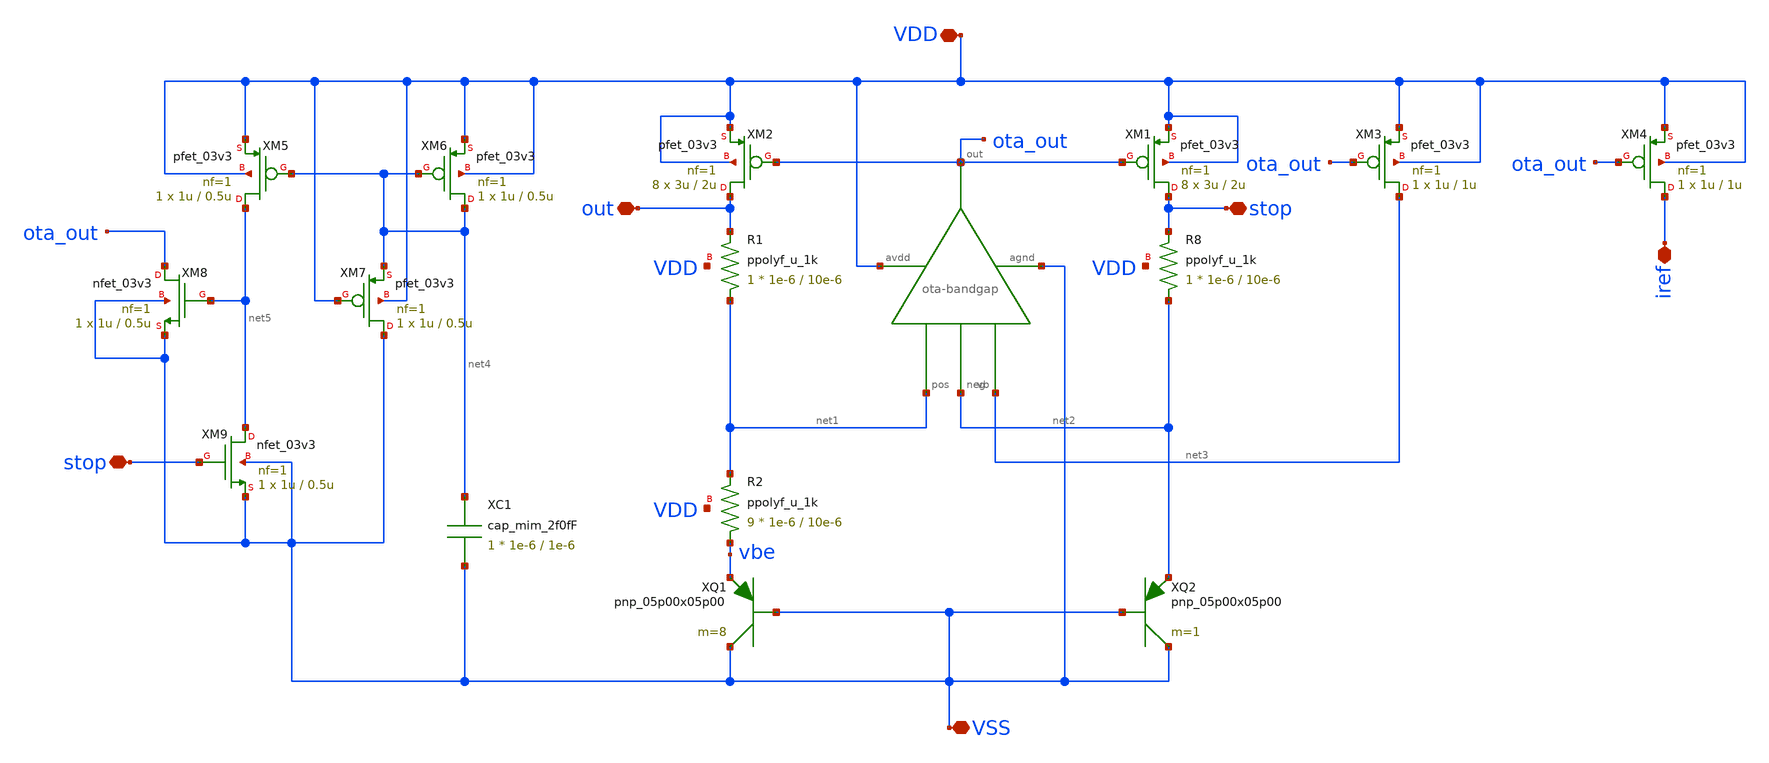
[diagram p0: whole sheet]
** sch_path: LDO/xschem/bandgap/symbol/bandgap.sch

.include $env(PDK_ROOT)/$env(PDK)/libs.tech/ngspice/design.ngspice
.lib $env(PDK_ROOT)/$env(PDK)/libs.tech/ngspice/sm141064.ngspice typical
.lib $env(PDK_ROOT)/$env(PDK)/libs.tech/ngspice/sm141064.ngspice mimcap_statistical
.lib $env(PDK_ROOT)/$env(PDK)/libs.tech/ngspice/sm141064.ngspice cap_mim
.lib $env(PDK_ROOT)/$env(PDK)/libs.tech/ngspice/sm141064.ngspice res_typical
.lib $env(PDK_ROOT)/$env(PDK)/libs.tech/ngspice/sm141064.ngspice bjt_typical
.lib $env(PDK_ROOT)/$env(PDK)/libs.tech/ngspice/sm141064.ngspice moscap_typical

**.subckt bandgap VDD VSS out iref stop stop
*.iopin VDD
*.iopin VSS
*.iopin out
*.iopin iref
*.iopin stop
*.iopin stop
XM1 stop ota_out VDD VDD pfet_03v3 L=2u W=3u nf=1 ad='int((nf+1)/2) * W/nf * 0.18u' as='int((nf+2)/2) * W/nf * 0.18u'
+ pd='2*int((nf+1)/2) * (W/nf + 0.18u)' ps='2*int((nf+2)/2) * (W/nf + 0.18u)' nrd='0.18u / W' nrs='0.18u / W'
+ sa=0 sb=0 sd=0 m=8
XM2 out ota_out VDD VDD pfet_03v3 L=2u W=3u nf=1 ad='int((nf+1)/2) * W/nf * 0.18u' as='int((nf+2)/2) * W/nf * 0.18u'
+ pd='2*int((nf+1)/2) * (W/nf + 0.18u)' ps='2*int((nf+2)/2) * (W/nf + 0.18u)' nrd='0.18u / W' nrs='0.18u / W'
+ sa=0 sb=0 sd=0 m=8
X1 ota_out VSS VDD net1 net2 net3 ota-bandgap
XQ1 VSS VSS vbe pnp_05p00x05p00 m=8
XQ2 VSS VSS net2 pnp_05p00x05p00 m=1
XR8 net2 stop VDD ppolyf_u_1k r_width=1e-6 r_length=10e-6 m=1
XR1 net1 out VDD ppolyf_u_1k r_width=1e-6 r_length=10e-6 m=1
XR2 vbe net1 VDD ppolyf_u_1k r_width=1e-6 r_length=10e-6 m=9
XM3 net3 ota_out VDD VDD pfet_03v3 L=1u W=1u nf=1 ad='int((nf+1)/2) * W/nf * 0.18u' as='int((nf+2)/2) * W/nf * 0.18u'
+ pd='2*int((nf+1)/2) * (W/nf + 0.18u)' ps='2*int((nf+2)/2) * (W/nf + 0.18u)' nrd='0.18u / W' nrs='0.18u / W'
+ sa=0 sb=0 sd=0 m=1
XM4 iref ota_out VDD VDD pfet_03v3 L=1u W=1u nf=1 ad='int((nf+1)/2) * W/nf * 0.18u' as='int((nf+2)/2) * W/nf * 0.18u'
+ pd='2*int((nf+1)/2) * (W/nf + 0.18u)' ps='2*int((nf+2)/2) * (W/nf + 0.18u)' nrd='0.18u / W' nrs='0.18u / W'
+ sa=0 sb=0 sd=0 m=1
XM6 net4 net4 VDD VDD pfet_03v3 L=0.5u W=1u nf=1 ad='int((nf+1)/2) * W/nf * 0.18u' as='int((nf+2)/2) * W/nf * 0.18u'
+ pd='2*int((nf+1)/2) * (W/nf + 0.18u)' ps='2*int((nf+2)/2) * (W/nf + 0.18u)' nrd='0.18u / W' nrs='0.18u / W'
+ sa=0 sb=0 sd=0 m=1
XM5 net5 net4 VDD VDD pfet_03v3 L=0.5u W=1u nf=1 ad='int((nf+1)/2) * W/nf * 0.18u' as='int((nf+2)/2) * W/nf * 0.18u'
+ pd='2*int((nf+1)/2) * (W/nf + 0.18u)' ps='2*int((nf+2)/2) * (W/nf + 0.18u)' nrd='0.18u / W' nrs='0.18u / W'
+ sa=0 sb=0 sd=0 m=1
XM7 VSS VDD net4 VDD pfet_03v3 L=0.5u W=1u nf=1 ad='int((nf+1)/2) * W/nf * 0.18u' as='int((nf+2)/2) * W/nf * 0.18u'
+ pd='2*int((nf+1)/2) * (W/nf + 0.18u)' ps='2*int((nf+2)/2) * (W/nf + 0.18u)' nrd='0.18u / W' nrs='0.18u / W'
+ sa=0 sb=0 sd=0 m=1
XM8 ota_out net5 VSS VSS nfet_03v3 L=0.5u W=1u nf=1 ad='int((nf+1)/2) * W/nf * 0.18u' as='int((nf+2)/2) * W/nf * 0.18u'
+ pd='2*int((nf+1)/2) * (W/nf + 0.18u)' ps='2*int((nf+2)/2) * (W/nf + 0.18u)' nrd='0.18u / W' nrs='0.18u / W'
+ sa=0 sb=0 sd=0 m=1
XM9 net5 stop VSS VSS nfet_03v3 L=0.5u W=1u nf=1 ad='int((nf+1)/2) * W/nf * 0.18u' as='int((nf+2)/2) * W/nf * 0.18u'
+ pd='2*int((nf+1)/2) * (W/nf + 0.18u)' ps='2*int((nf+2)/2) * (W/nf + 0.18u)' nrd='0.18u / W' nrs='0.18u / W'
+ sa=0 sb=0 sd=0 m=1
XC1 net4 VSS cap_mim_2f0fF c_width=1e-6 c_length=1e-6 m=1
**.ends
.end
